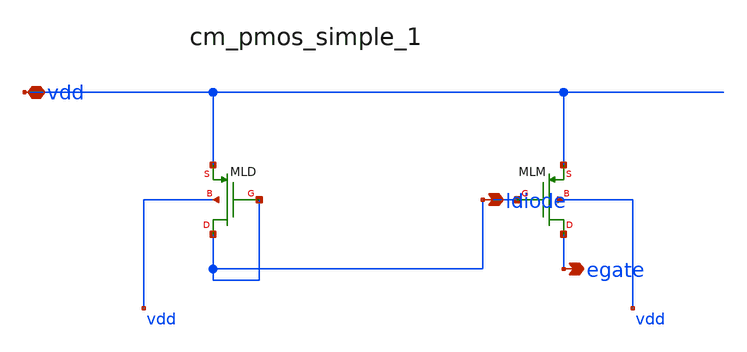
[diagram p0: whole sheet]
** sch_path: analog-db/raw/ldo_008_fer_mirror_ota/hier/blocks/cm_pmos_simple_1.sch
**.subckt cm_pmos_simple_1 vdd ldiode egate
*.iopin vdd
*.opin ldiode
*.opin egate
XMLD ldiode ldiode vdd vdd sg13_lv_pmos w=x_dut_xmld_w l=x_dut_xmld_l ng=1 m=x_dut_xmld_m
XMLM egate ldiode vdd vdd sg13_lv_pmos w=x_dut_xmlm_w l=x_dut_xmlm_l ng=1 m=x_dut_xmlm_m
**.ends
.end
